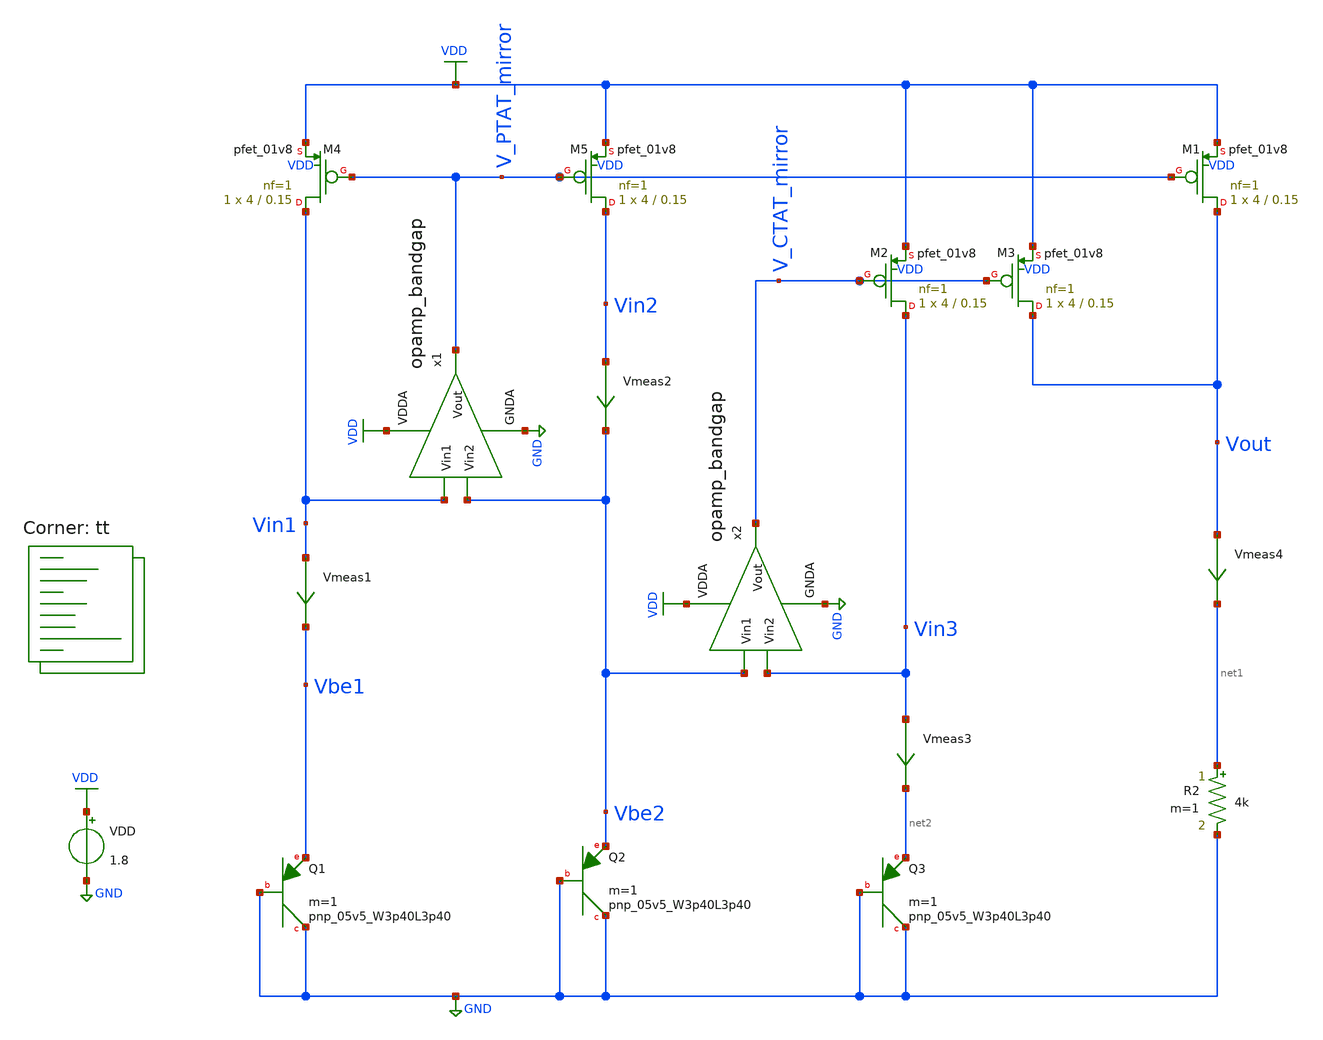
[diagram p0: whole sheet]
** sch_path: projects/pll/bandgapref/xschem_ngspice/mos_bandgap4.sch
**.subckt mos_bandgap4
XM4 Vin1 V_PTAT_mirror VDD VDD sky130_fd_pr__pfet_01v8 L=0.15 W=4 nf=1 ad='int((nf+1)/2) * W/nf * 0.29'
+ as='int((nf+2)/2) * W/nf * 0.29' pd='2*int((nf+1)/2) * (W/nf + 0.29)' ps='2*int((nf+2)/2) * (W/nf + 0.29)'
+ nrd='0.29 / W' nrs='0.29 / W' sa=0 sb=0 sd=0 mult=1 m=1
XM5 Vin2 V_PTAT_mirror VDD VDD sky130_fd_pr__pfet_01v8 L=0.15 W=4 nf=1 ad='int((nf+1)/2) * W/nf * 0.29'
+ as='int((nf+2)/2) * W/nf * 0.29' pd='2*int((nf+1)/2) * (W/nf + 0.29)' ps='2*int((nf+2)/2) * (W/nf + 0.29)'
+ nrd='0.29 / W' nrs='0.29 / W' sa=0 sb=0 sd=0 mult=1 m=1
XQ1 GND GND Vbe1 sky130_fd_pr__pnp_05v5_W3p40L3p40 m=1
XQ2 GND GND Vbe2 sky130_fd_pr__pnp_05v5_W3p40L3p40 m=1
XM1 Vout V_PTAT_mirror VDD VDD sky130_fd_pr__pfet_01v8 L=0.15 W=4 nf=1 ad='int((nf+1)/2) * W/nf * 0.29'
+ as='int((nf+2)/2) * W/nf * 0.29' pd='2*int((nf+1)/2) * (W/nf + 0.29)' ps='2*int((nf+2)/2) * (W/nf + 0.29)'
+ nrd='0.29 / W' nrs='0.29 / W' sa=0 sb=0 sd=0 mult=1 m=1
R2 net1 GND 4k m=1
Vmeas4 Vout net1 0
.save i(vmeas4)
x1 VDD V_PTAT_mirror Vbe2 Vin1 GND opamp_bandgap
Vmeas1 Vin1 Vbe1 0
.save i(vmeas1)
Vmeas2 Vin2 Vbe2 0
.save i(vmeas2)
x2 VDD V_CTAT_mirror Vin3 Vbe2 GND opamp_bandgap
Vmeas3 Vin3 net2 0
.save i(vmeas3)
XM2 Vin3 V_CTAT_mirror VDD VDD sky130_fd_pr__pfet_01v8 L=0.15 W=4 nf=1 ad='int((nf+1)/2) * W/nf * 0.29'
+ as='int((nf+2)/2) * W/nf * 0.29' pd='2*int((nf+1)/2) * (W/nf + 0.29)' ps='2*int((nf+2)/2) * (W/nf + 0.29)'
+ nrd='0.29 / W' nrs='0.29 / W' sa=0 sb=0 sd=0 mult=1 m=1
XM3 Vout V_CTAT_mirror VDD VDD sky130_fd_pr__pfet_01v8 L=0.15 W=4 nf=1 ad='int((nf+1)/2) * W/nf * 0.29'
+ as='int((nf+2)/2) * W/nf * 0.29' pd='2*int((nf+1)/2) * (W/nf + 0.29)' ps='2*int((nf+2)/2) * (W/nf + 0.29)'
+ nrd='0.29 / W' nrs='0.29 / W' sa=0 sb=0 sd=0 mult=1 m=1
VDD VDD GND 1.8
XQ3 GND GND net2 sky130_fd_pr__pnp_05v5_W3p40L3p40 m=1
**** begin user architecture code
.lib $::SKYWATER_MODELS/sky130.lib.spice tt



.option wnflag=1

* .param VDDGAUSS = agauss(1.8, 0.05, 1)
* .param VDD = VDDGAUSS
.param VDD = 1.8

* .param TEMPGAUSS = agauss(40, 30, 1)
* .param temp = TEMPGAUSS
.option temp = 26

.control
  save all
  op
  dc temp -40 120 1 VDD 1.8 5 0.1
  write mos_bandgap4.raw
  set appendwrite
.endc



**** end user architecture code
**.ends

* expanding   symbol:
*+  /foss/designs/my_design/projects/pll/bandgapref/xschem_ngspice/opamp_bandgap.sym # of pins=5
** sym_path: projects/pll/bandgapref/xschem_ngspice/opamp_bandgap.sym
** sch_path: projects/pll/bandgapref/xschem_ngspice/opamp_bandgap.sch
.subckt opamp_bandgap VDDA Vout Vin2 Vin1 GNDA
*.ipin Vin1
*.opin Vout
*.ipin Vin2
*.ipin GNDA
*.ipin VDDA
XM2 net1 Vin1 net2 GNDA sky130_fd_pr__nfet_01v8 L=0.15 W=1 nf=1 ad='int((nf+1)/2) * W/nf * 0.29' as='int((nf+2)/2) * W/nf * 0.29'
+ pd='2*int((nf+1)/2) * (W/nf + 0.29)' ps='2*int((nf+2)/2) * (W/nf + 0.29)' nrd='0.29 / W' nrs='0.29 / W'
+ sa=0 sb=0 sd=0 mult=1 m=1
XM3 Vout Vin2 net2 GNDA sky130_fd_pr__nfet_01v8 L=0.15 W=1 nf=1 ad='int((nf+1)/2) * W/nf * 0.29' as='int((nf+2)/2) * W/nf * 0.29'
+ pd='2*int((nf+1)/2) * (W/nf + 0.29)' ps='2*int((nf+2)/2) * (W/nf + 0.29)' nrd='0.29 / W' nrs='0.29 / W'
+ sa=0 sb=0 sd=0 mult=1 m=1
XM4 net1 net1 VDDA VDDA sky130_fd_pr__pfet_01v8 L=0.15 W=2 nf=1 ad='int((nf+1)/2) * W/nf * 0.29' as='int((nf+2)/2) * W/nf * 0.29'
+ pd='2*int((nf+1)/2) * (W/nf + 0.29)' ps='2*int((nf+2)/2) * (W/nf + 0.29)' nrd='0.29 / W' nrs='0.29 / W'
+ sa=0 sb=0 sd=0 mult=1 m=1
XM5 Vout net1 VDDA VDDA sky130_fd_pr__pfet_01v8 L=0.15 W=2 nf=1 ad='int((nf+1)/2) * W/nf * 0.29' as='int((nf+2)/2) * W/nf * 0.29'
+ pd='2*int((nf+1)/2) * (W/nf + 0.29)' ps='2*int((nf+2)/2) * (W/nf + 0.29)' nrd='0.29 / W' nrs='0.29 / W'
+ sa=0 sb=0 sd=0 mult=1 m=1
XM1 net2 net2 GNDA GNDA sky130_fd_pr__nfet_01v8 L=0.15 W=1 nf=1 ad='int((nf+1)/2) * W/nf * 0.29' as='int((nf+2)/2) * W/nf * 0.29'
+ pd='2*int((nf+1)/2) * (W/nf + 0.29)' ps='2*int((nf+2)/2) * (W/nf + 0.29)' nrd='0.29 / W' nrs='0.29 / W'
+ sa=0 sb=0 sd=0 mult=1 m=1
.ends

.GLOBAL GND
.GLOBAL VDD
.end
